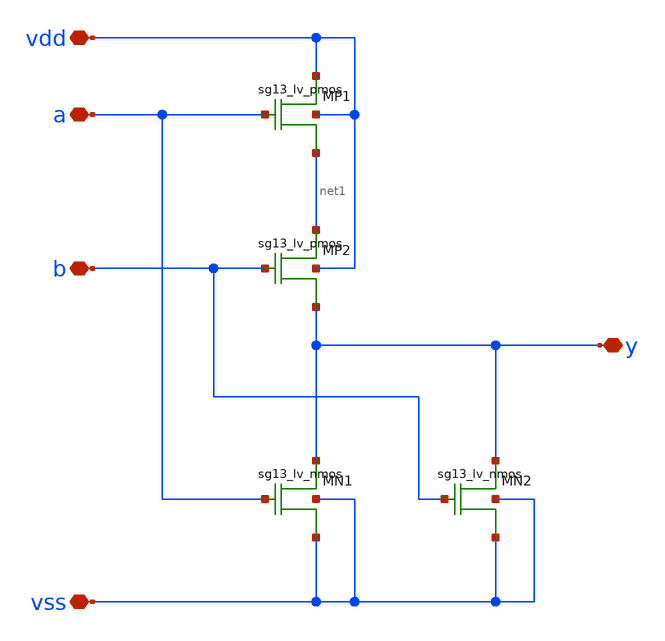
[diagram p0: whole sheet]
** sch_path: xschem/logic_gates/NORLV.sch
**.subckt NORLV vdd vss y a b
*.iopin vdd
*.iopin vss
*.iopin y
*.iopin a
*.iopin b
XMP1 vdd a net1 vdd sg13_lv_pmos w=2.0u l=0.13u ng=1 m=1
XMP2 net1 b y vdd sg13_lv_pmos w=2.0u l=0.13u ng=1 m=1
XMN1 y a vss vss sg13_lv_nmos w=0.5u l=0.13u ng=1 m=1
XMN2 y b vss vss sg13_lv_nmos w=0.5u l=0.13u ng=1 m=1
**.ends
.end
